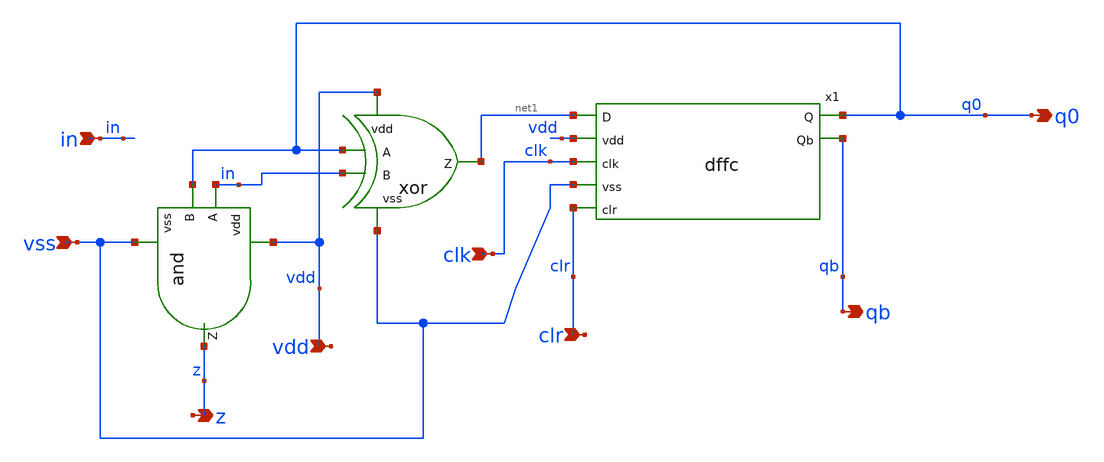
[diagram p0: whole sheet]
** sch_path: track_vlsi/lado/sch/counter1b.sch
**.subckt counter1b vss clk vdd clr q0 qb z in
*.ipin vss
*.ipin clk
*.ipin vdd
*.ipin clr
*.opin q0
*.opin qb
*.opin z
*.ipin in
x1 net1 q0 vdd clk vss qb clr dffc
xor vdd q0 in net1 vss xor
x2 vdd in q0 z vss and
**.ends

* expanding   symbol:  /home/eamta/eamta2021/sch/dffc/dffc.sym # of pins=7
** sym_path: track_vlsi/lado/sch/dffc.sym
** sch_path: track_vlsi/lado/sch/dffc.sch
.subckt dffc D Q vdd clk vss Qb clr
*.ipin clk
*.ipin vdd
*.ipin vss
*.ipin D
*.opin Q
*.opin Qb
*.ipin clr
XM0 net1 nclk D vdd sky130_fd_pr__pfet_01v8 L=0.15 W=1.5 nf=1 ad='int((nf+1)/2) * W/nf * 0.29' as='int((nf+2)/2) * W/nf * 0.29'
+ pd='2*int((nf+1)/2) * (W/nf + 0.29)' ps='2*int((nf+2)/2) * (W/nf + 0.29)' nrd='0.29 / W' nrs='0.29 / W'
+ sa=0 sb=0 sd=0 mult=1 m=1
XM1 net1 clk D vss sky130_fd_pr__nfet_01v8 L=0.15 W=1.5 nf=1 ad='int((nf+1)/2) * W/nf * 0.29' as='int((nf+2)/2) * W/nf * 0.29'
+ pd='2*int((nf+1)/2) * (W/nf + 0.29)' ps='2*int((nf+2)/2) * (W/nf + 0.29)' nrd='0.29 / W' nrs='0.29 / W'
+ sa=0 sb=0 sd=0 mult=1 m=1
XM2 net2 net4 vdd vdd sky130_fd_pr__pfet_01v8 L=0.15 W=1.5 nf=1 ad='int((nf+1)/2) * W/nf * 0.29' as='int((nf+2)/2) * W/nf * 0.29'
+ pd='2*int((nf+1)/2) * (W/nf + 0.29)' ps='2*int((nf+2)/2) * (W/nf + 0.29)' nrd='0.29 / W' nrs='0.29 / W'
+ sa=0 sb=0 sd=0 mult=1 m=1
XM5 net3 clr vss vss sky130_fd_pr__nfet_01v8 L=0.15 W=1.5 nf=1 ad='int((nf+1)/2) * W/nf * 0.29' as='int((nf+2)/2) * W/nf * 0.29'
+ pd='2*int((nf+1)/2) * (W/nf + 0.29)' ps='2*int((nf+2)/2) * (W/nf + 0.29)' nrd='0.29 / W' nrs='0.29 / W'
+ sa=0 sb=0 sd=0 mult=1 m=1
XM6 net3 clr net2 vdd sky130_fd_pr__pfet_01v8 L=0.15 W=1.5 nf=1 ad='int((nf+1)/2) * W/nf * 0.29' as='int((nf+2)/2) * W/nf * 0.29'
+ pd='2*int((nf+1)/2) * (W/nf + 0.29)' ps='2*int((nf+2)/2) * (W/nf + 0.29)' nrd='0.29 / W' nrs='0.29 / W'
+ sa=0 sb=0 sd=0 mult=1 m=1
XM14 net5 clk net4 vdd sky130_fd_pr__pfet_01v8 L=0.15 W=1.5 nf=1 ad='int((nf+1)/2) * W/nf * 0.29' as='int((nf+2)/2) * W/nf * 0.29'
+ pd='2*int((nf+1)/2) * (W/nf + 0.29)' ps='2*int((nf+2)/2) * (W/nf + 0.29)' nrd='0.29 / W' nrs='0.29 / W'
+ sa=0 sb=0 sd=0 mult=1 m=1
XM15 net5 nclk net4 vss sky130_fd_pr__nfet_01v8 L=0.15 W=1.5 nf=1 ad='int((nf+1)/2) * W/nf * 0.29' as='int((nf+2)/2) * W/nf * 0.29'
+ pd='2*int((nf+1)/2) * (W/nf + 0.29)' ps='2*int((nf+2)/2) * (W/nf + 0.29)' nrd='0.29 / W' nrs='0.29 / W'
+ sa=0 sb=0 sd=0 mult=1 m=1
XM7 net3 net4 vss vss sky130_fd_pr__nfet_01v8 L=0.15 W=1.5 nf=1 ad='int((nf+1)/2) * W/nf * 0.29' as='int((nf+2)/2) * W/nf * 0.29'
+ pd='2*int((nf+1)/2) * (W/nf + 0.29)' ps='2*int((nf+2)/2) * (W/nf + 0.29)' nrd='0.29 / W' nrs='0.29 / W'
+ sa=0 sb=0 sd=0 mult=1 m=1
XM3 net3 clk net1 vdd sky130_fd_pr__pfet_01v8 L=0.15 W=1.5 nf=1 ad='int((nf+1)/2) * W/nf * 0.29' as='int((nf+2)/2) * W/nf * 0.29'
+ pd='2*int((nf+1)/2) * (W/nf + 0.29)' ps='2*int((nf+2)/2) * (W/nf + 0.29)' nrd='0.29 / W' nrs='0.29 / W'
+ sa=0 sb=0 sd=0 mult=1 m=1
XM4 net3 nclk net1 vss sky130_fd_pr__nfet_01v8 L=0.15 W=1.5 nf=1 ad='int((nf+1)/2) * W/nf * 0.29' as='int((nf+2)/2) * W/nf * 0.29'
+ pd='2*int((nf+1)/2) * (W/nf + 0.29)' ps='2*int((nf+2)/2) * (W/nf + 0.29)' nrd='0.29 / W' nrs='0.29 / W'
+ sa=0 sb=0 sd=0 mult=1 m=1
XM8 net6 clr vdd vdd sky130_fd_pr__pfet_01v8 L=0.15 W=1.5 nf=1 ad='int((nf+1)/2) * W/nf * 0.29' as='int((nf+2)/2) * W/nf * 0.29'
+ pd='2*int((nf+1)/2) * (W/nf + 0.29)' ps='2*int((nf+2)/2) * (W/nf + 0.29)' nrd='0.29 / W' nrs='0.29 / W'
+ sa=0 sb=0 sd=0 mult=1 m=1
XM9 Q net5 vss vss sky130_fd_pr__nfet_01v8 L=0.15 W=1.5 nf=1 ad='int((nf+1)/2) * W/nf * 0.29' as='int((nf+2)/2) * W/nf * 0.29'
+ pd='2*int((nf+1)/2) * (W/nf + 0.29)' ps='2*int((nf+2)/2) * (W/nf + 0.29)' nrd='0.29 / W' nrs='0.29 / W'
+ sa=0 sb=0 sd=0 mult=1 m=1
XM10 Q net5 net6 vdd sky130_fd_pr__pfet_01v8 L=0.15 W=1.5 nf=1 ad='int((nf+1)/2) * W/nf * 0.29' as='int((nf+2)/2) * W/nf * 0.29'
+ pd='2*int((nf+1)/2) * (W/nf + 0.29)' ps='2*int((nf+2)/2) * (W/nf + 0.29)' nrd='0.29 / W' nrs='0.29 / W'
+ sa=0 sb=0 sd=0 mult=1 m=1
XM11 Q clr vss vss sky130_fd_pr__nfet_01v8 L=0.15 W=1.5 nf=1 ad='int((nf+1)/2) * W/nf * 0.29' as='int((nf+2)/2) * W/nf * 0.29'
+ pd='2*int((nf+1)/2) * (W/nf + 0.29)' ps='2*int((nf+2)/2) * (W/nf + 0.29)' nrd='0.29 / W' nrs='0.29 / W'
+ sa=0 sb=0 sd=0 mult=1 m=1
XM12 Qb nclk net5 vdd sky130_fd_pr__pfet_01v8 L=0.15 W=1.5 nf=1 ad='int((nf+1)/2) * W/nf * 0.29' as='int((nf+2)/2) * W/nf * 0.29'
+ pd='2*int((nf+1)/2) * (W/nf + 0.29)' ps='2*int((nf+2)/2) * (W/nf + 0.29)' nrd='0.29 / W' nrs='0.29 / W'
+ sa=0 sb=0 sd=0 mult=1 m=1
XM13 Qb clk net5 vss sky130_fd_pr__nfet_01v8 L=0.15 W=1.5 nf=1 ad='int((nf+1)/2) * W/nf * 0.29' as='int((nf+2)/2) * W/nf * 0.29'
+ pd='2*int((nf+1)/2) * (W/nf + 0.29)' ps='2*int((nf+2)/2) * (W/nf + 0.29)' nrd='0.29 / W' nrs='0.29 / W'
+ sa=0 sb=0 sd=0 mult=1 m=1
XM16 nclk clk vdd vdd sky130_fd_pr__pfet_01v8 L=0.15 W=1.5 nf=1 ad='int((nf+1)/2) * W/nf * 0.29' as='int((nf+2)/2) * W/nf * 0.29'
+ pd='2*int((nf+1)/2) * (W/nf + 0.29)' ps='2*int((nf+2)/2) * (W/nf + 0.29)' nrd='0.29 / W' nrs='0.29 / W'
+ sa=0 sb=0 sd=0 mult=1 m=1
XM17 nclk clk vss vss sky130_fd_pr__nfet_01v8 L=0.15 W=1.5 nf=1 ad='int((nf+1)/2) * W/nf * 0.29' as='int((nf+2)/2) * W/nf * 0.29'
+ pd='2*int((nf+1)/2) * (W/nf + 0.29)' ps='2*int((nf+2)/2) * (W/nf + 0.29)' nrd='0.29 / W' nrs='0.29 / W'
+ sa=0 sb=0 sd=0 mult=1 m=1
XM18 net4 net1 vdd vdd sky130_fd_pr__pfet_01v8 L=0.15 W=1.5 nf=1 ad='int((nf+1)/2) * W/nf * 0.29' as='int((nf+2)/2) * W/nf * 0.29'
+ pd='2*int((nf+1)/2) * (W/nf + 0.29)' ps='2*int((nf+2)/2) * (W/nf + 0.29)' nrd='0.29 / W' nrs='0.29 / W'
+ sa=0 sb=0 sd=0 mult=1 m=1
XM19 net4 net1 vss vss sky130_fd_pr__nfet_01v8 L=0.15 W=1.5 nf=1 ad='int((nf+1)/2) * W/nf * 0.29' as='int((nf+2)/2) * W/nf * 0.29'
+ pd='2*int((nf+1)/2) * (W/nf + 0.29)' ps='2*int((nf+2)/2) * (W/nf + 0.29)' nrd='0.29 / W' nrs='0.29 / W'
+ sa=0 sb=0 sd=0 mult=1 m=1
XM20 Qb Q vdd vdd sky130_fd_pr__pfet_01v8 L=0.15 W=1.5 nf=1 ad='int((nf+1)/2) * W/nf * 0.29' as='int((nf+2)/2) * W/nf * 0.29'
+ pd='2*int((nf+1)/2) * (W/nf + 0.29)' ps='2*int((nf+2)/2) * (W/nf + 0.29)' nrd='0.29 / W' nrs='0.29 / W'
+ sa=0 sb=0 sd=0 mult=1 m=1
XM21 Qb Q vss vss sky130_fd_pr__nfet_01v8 L=0.15 W=1.5 nf=1 ad='int((nf+1)/2) * W/nf * 0.29' as='int((nf+2)/2) * W/nf * 0.29'
+ pd='2*int((nf+1)/2) * (W/nf + 0.29)' ps='2*int((nf+2)/2) * (W/nf + 0.29)' nrd='0.29 / W' nrs='0.29 / W'
+ sa=0 sb=0 sd=0 mult=1 m=1
.ends


* expanding   symbol:  /home/eamta/eamta2021/sch/xor/xor.sym # of pins=5
** sym_path: track_vlsi/lado/sch/xor.sym
** sch_path: track_vlsi/lado/sch/xor.sch
.subckt xor vdd A B Z vss
*.ipin A
*.ipin vss
*.ipin vdd
*.opin Z
*.ipin B
XM0 net1 Bb vdd vdd sky130_fd_pr__pfet_01v8 L=0.15 W=0.9 nf=1 ad='int((nf+1)/2) * W/nf * 0.29' as='int((nf+2)/2) * W/nf * 0.29'
+ pd='2*int((nf+1)/2) * (W/nf + 0.29)' ps='2*int((nf+2)/2) * (W/nf + 0.29)' nrd='0.29 / W' nrs='0.29 / W'
+ sa=0 sb=0 sd=0 mult=1 m=1
XM5 Z A net3 vss sky130_fd_pr__nfet_01v8 L=0.15 W=0.9 nf=1 ad='int((nf+1)/2) * W/nf * 0.29' as='int((nf+2)/2) * W/nf * 0.29'
+ pd='2*int((nf+1)/2) * (W/nf + 0.29)' ps='2*int((nf+2)/2) * (W/nf + 0.29)' nrd='0.29 / W' nrs='0.29 / W'
+ sa=0 sb=0 sd=0 mult=1 m=1
XM1 net1 Ab vdd vdd sky130_fd_pr__pfet_01v8 L=0.15 W=0.9 nf=1 ad='int((nf+1)/2) * W/nf * 0.29' as='int((nf+2)/2) * W/nf * 0.29'
+ pd='2*int((nf+1)/2) * (W/nf + 0.29)' ps='2*int((nf+2)/2) * (W/nf + 0.29)' nrd='0.29 / W' nrs='0.29 / W'
+ sa=0 sb=0 sd=0 mult=1 m=1
XM2 Z A net1 vdd sky130_fd_pr__pfet_01v8 L=0.15 W=0.9 nf=1 ad='int((nf+1)/2) * W/nf * 0.29' as='int((nf+2)/2) * W/nf * 0.29'
+ pd='2*int((nf+1)/2) * (W/nf + 0.29)' ps='2*int((nf+2)/2) * (W/nf + 0.29)' nrd='0.29 / W' nrs='0.29 / W'
+ sa=0 sb=0 sd=0 mult=1 m=1
XM4 Z Ab net2 vss sky130_fd_pr__nfet_01v8 L=0.15 W=0.9 nf=1 ad='int((nf+1)/2) * W/nf * 0.29' as='int((nf+2)/2) * W/nf * 0.29'
+ pd='2*int((nf+1)/2) * (W/nf + 0.29)' ps='2*int((nf+2)/2) * (W/nf + 0.29)' nrd='0.29 / W' nrs='0.29 / W'
+ sa=0 sb=0 sd=0 mult=1 m=1
XM6 net2 Bb vss vss sky130_fd_pr__nfet_01v8 L=0.15 W=0.9 nf=1 ad='int((nf+1)/2) * W/nf * 0.29' as='int((nf+2)/2) * W/nf * 0.29'
+ pd='2*int((nf+1)/2) * (W/nf + 0.29)' ps='2*int((nf+2)/2) * (W/nf + 0.29)' nrd='0.29 / W' nrs='0.29 / W'
+ sa=0 sb=0 sd=0 mult=1 m=1
XM8 Ab A vdd vdd sky130_fd_pr__pfet_01v8 L=0.15 W=0.9 nf=1 ad='int((nf+1)/2) * W/nf * 0.29' as='int((nf+2)/2) * W/nf * 0.29'
+ pd='2*int((nf+1)/2) * (W/nf + 0.29)' ps='2*int((nf+2)/2) * (W/nf + 0.29)' nrd='0.29 / W' nrs='0.29 / W'
+ sa=0 sb=0 sd=0 mult=1 m=1
XM9 Ab A vss vss sky130_fd_pr__nfet_01v8 L=0.15 W=0.45 nf=1 ad='int((nf+1)/2) * W/nf * 0.29' as='int((nf+2)/2) * W/nf * 0.29'
+ pd='2*int((nf+1)/2) * (W/nf + 0.29)' ps='2*int((nf+2)/2) * (W/nf + 0.29)' nrd='0.29 / W' nrs='0.29 / W'
+ sa=0 sb=0 sd=0 mult=1 m=1
XM3 Z B net1 vdd sky130_fd_pr__pfet_01v8 L=0.15 W=0.9 nf=1 ad='int((nf+1)/2) * W/nf * 0.29' as='int((nf+2)/2) * W/nf * 0.29'
+ pd='2*int((nf+1)/2) * (W/nf + 0.29)' ps='2*int((nf+2)/2) * (W/nf + 0.29)' nrd='0.29 / W' nrs='0.29 / W'
+ sa=0 sb=0 sd=0 mult=1 m=1
XM12 Bb B vss vss sky130_fd_pr__nfet_01v8 L=0.15 W=0.45 nf=1 ad='int((nf+1)/2) * W/nf * 0.29' as='int((nf+2)/2) * W/nf * 0.29'
+ pd='2*int((nf+1)/2) * (W/nf + 0.29)' ps='2*int((nf+2)/2) * (W/nf + 0.29)' nrd='0.29 / W' nrs='0.29 / W'
+ sa=0 sb=0 sd=0 mult=1 m=1
XM7 net3 B vss vss sky130_fd_pr__nfet_01v8 L=0.15 W=0.9 nf=1 ad='int((nf+1)/2) * W/nf * 0.29' as='int((nf+2)/2) * W/nf * 0.29'
+ pd='2*int((nf+1)/2) * (W/nf + 0.29)' ps='2*int((nf+2)/2) * (W/nf + 0.29)' nrd='0.29 / W' nrs='0.29 / W'
+ sa=0 sb=0 sd=0 mult=1 m=1
XM10 Bb B vdd vdd sky130_fd_pr__pfet_01v8 L=0.15 W=0.9 nf=1 ad='int((nf+1)/2) * W/nf * 0.29' as='int((nf+2)/2) * W/nf * 0.29'
+ pd='2*int((nf+1)/2) * (W/nf + 0.29)' ps='2*int((nf+2)/2) * (W/nf + 0.29)' nrd='0.29 / W' nrs='0.29 / W'
+ sa=0 sb=0 sd=0 mult=1 m=1
.ends


* expanding   symbol:  /home/eamta/eamta2021/sch/and/and.sym # of pins=5
** sym_path: track_vlsi/lado/sch/and.sym
** sch_path: track_vlsi/lado/sch/and.sch
.subckt and vdd A B Z vss
*.opin Z
*.ipin vdd
*.ipin A
*.ipin vss
*.ipin B
XM1 Z net1 vdd vdd sky130_fd_pr__pfet_01v8 L=0.15 W=0.9 nf=1 ad='int((nf+1)/2) * W/nf * 0.29' as='int((nf+2)/2) * W/nf * 0.29'
+ pd='2*int((nf+1)/2) * (W/nf + 0.29)' ps='2*int((nf+2)/2) * (W/nf + 0.29)' nrd='0.29 / W' nrs='0.29 / W'
+ sa=0 sb=0 sd=0 mult=1 m=1
XM2 Z net1 vss vss sky130_fd_pr__nfet_01v8 L=0.15 W=0.45 nf=1 ad='int((nf+1)/2) * W/nf * 0.29' as='int((nf+2)/2) * W/nf * 0.29'
+ pd='2*int((nf+1)/2) * (W/nf + 0.29)' ps='2*int((nf+2)/2) * (W/nf + 0.29)' nrd='0.29 / W' nrs='0.29 / W'
+ sa=0 sb=0 sd=0 mult=1 m=1
XM3 net1 A vdd vdd sky130_fd_pr__pfet_01v8 L=0.15 W=0.9 nf=1 ad='int((nf+1)/2) * W/nf * 0.29' as='int((nf+2)/2) * W/nf * 0.29'
+ pd='2*int((nf+1)/2) * (W/nf + 0.29)' ps='2*int((nf+2)/2) * (W/nf + 0.29)' nrd='0.29 / W' nrs='0.29 / W'
+ sa=0 sb=0 sd=0 mult=1 m=1
XM4 net1 B vdd vdd sky130_fd_pr__pfet_01v8 L=0.15 W=0.9 nf=1 ad='int((nf+1)/2) * W/nf * 0.29' as='int((nf+2)/2) * W/nf * 0.29'
+ pd='2*int((nf+1)/2) * (W/nf + 0.29)' ps='2*int((nf+2)/2) * (W/nf + 0.29)' nrd='0.29 / W' nrs='0.29 / W'
+ sa=0 sb=0 sd=0 mult=1 m=1
XM5 net1 A net2 vss sky130_fd_pr__nfet_01v8 L=0.15 W=0.9 nf=1 ad='int((nf+1)/2) * W/nf * 0.29' as='int((nf+2)/2) * W/nf * 0.29'
+ pd='2*int((nf+1)/2) * (W/nf + 0.29)' ps='2*int((nf+2)/2) * (W/nf + 0.29)' nrd='0.29 / W' nrs='0.29 / W'
+ sa=0 sb=0 sd=0 mult=1 m=1
XM6 net2 B vss vss sky130_fd_pr__nfet_01v8 L=0.15 W=0.9 nf=1 ad='int((nf+1)/2) * W/nf * 0.29' as='int((nf+2)/2) * W/nf * 0.29'
+ pd='2*int((nf+1)/2) * (W/nf + 0.29)' ps='2*int((nf+2)/2) * (W/nf + 0.29)' nrd='0.29 / W' nrs='0.29 / W'
+ sa=0 sb=0 sd=0 mult=1 m=1
.ends

.end
